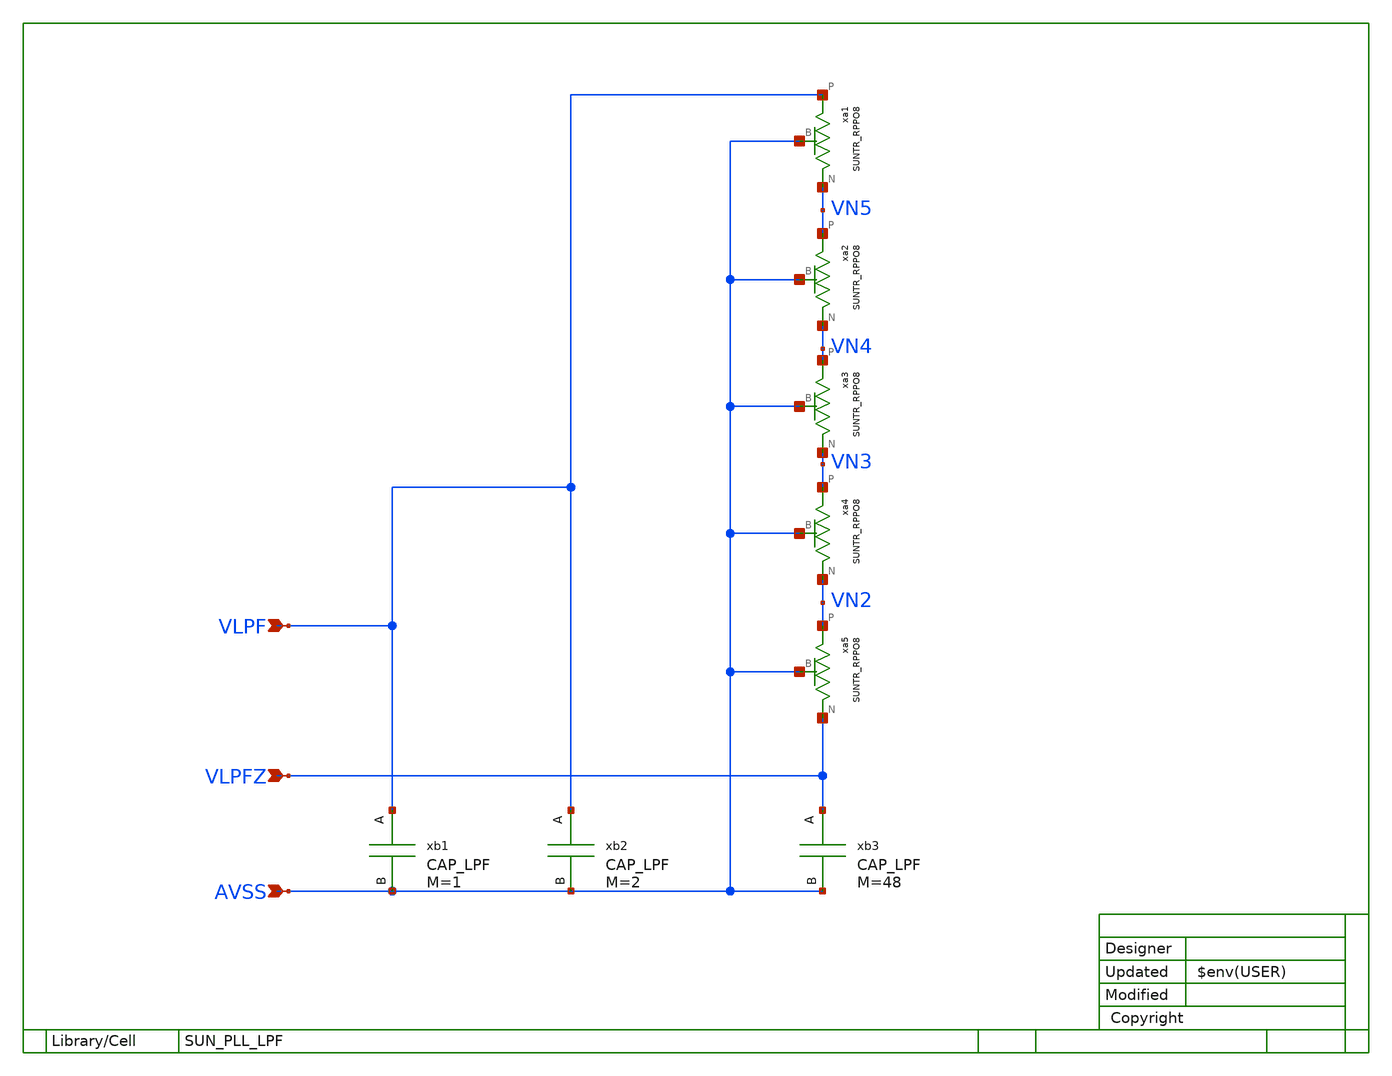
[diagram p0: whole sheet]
** sch_path: ip/sun_pll_sky130nm/design/SUN_PLL_SKY130NM/SUN_PLL_LPF.sch
**.subckt SUN_PLL_LPF VLPF AVSS VLPFZ
*.ipin VLPF
*.ipin AVSS
*.ipin VLPFZ
xa5 VLPFZ VN2 AVSS SUNTR_RPPO8 xoffset=0 yoffset=2 angle=0 M=1
xb3 VLPFZ AVSS CAP_LPF xoffset=0 yoffset=0 angle=0 M=48
xb2 VLPF AVSS CAP_LPF xoffset=0 yoffset=0 angle=0 M=2
xb1 VLPF AVSS CAP_LPF xoffset=0 yoffset=0 angle=0 M=1
xa4 VN2 VN3 AVSS SUNTR_RPPO8 xoffset=0 yoffset=2 angle=0 M=1
xa3 VN3 VN4 AVSS SUNTR_RPPO8 xoffset=0 yoffset=2 angle=0 M=1
xa2 VN4 VN5 AVSS SUNTR_RPPO8 xoffset=0 yoffset=2 angle=0 M=1
xa1 VN5 VLPF AVSS SUNTR_RPPO8 xoffset=0 yoffset=2 angle=0 M=1
**.ends

* expanding   symbol:  SUN_TR_SKY130NM/SUNTR_RPPO8.sym # of pins=3
** sym_path: ip/sun_tr_sky130nm/design/SUN_TR_SKY130NM/SUNTR_RPPO8.sym
** sch_path: ip/sun_tr_sky130nm/design/SUN_TR_SKY130NM/SUNTR_RPPO8.sch
.subckt SUNTR_RPPO8 N P B  xoffset=0 yoffset=0 angle=0 M=1
*.iopin P
*.iopin N
*.iopin B
XXA1 N P B SUNTR_RES8 xoffset=0 yoffset=0 angle=0
.ends


* expanding   symbol:  SUN_PLL_SKY130NM/CAP_LPF.sym # of pins=2
** sym_path: ip/sun_pll_sky130nm/design/SUN_PLL_SKY130NM/CAP_LPF.sym
** sch_path: ip/sun_pll_sky130nm/design/SUN_PLL_SKY130NM/CAP_LPF.sch
.subckt CAP_LPF A B  xoffset=0 yoffset=0 angle=0 M=1
*.iopin A
*.iopin B
R1 A NC0 sky130_fd_pr__res_generic_m1 W=0.4 L=0.4 m=1
R2 B NC1 sky130_fd_pr__res_generic_m1 W=0.4 L=0.4 m=1
.ends


* expanding   symbol:  SUN_TR_SKY130NM/SUNTR_RES8.sym # of pins=3
** sym_path: ip/sun_tr_sky130nm/design/SUN_TR_SKY130NM/SUNTR_RES8.sym
** sch_path: ip/sun_tr_sky130nm/design/SUN_TR_SKY130NM/SUNTR_RES8.sch
.subckt SUNTR_RES8 N P B  xoffset=0 yoffset=0 angle=0
*.iopin N
*.iopin P
*.iopin B
XR1_0 INT_0 N B sky130_fd_pr__res_high_po W=0.72 L=8.8 mult=1 m=1
XR1_1 INT_1 INT_0 B sky130_fd_pr__res_high_po W=0.72 L=8.8 mult=1 m=1
XR1_2 INT_2 INT_1 B sky130_fd_pr__res_high_po W=0.72 L=8.8 mult=1 m=1
XR1_3 INT_3 INT_2 B sky130_fd_pr__res_high_po W=0.72 L=8.8 mult=1 m=1
XR1_4 INT_4 INT_3 B sky130_fd_pr__res_high_po W=0.72 L=8.8 mult=1 m=1
XR1_5 INT_5 INT_4 B sky130_fd_pr__res_high_po W=0.72 L=8.8 mult=1 m=1
XR1_6 INT_6 INT_5 B sky130_fd_pr__res_high_po W=0.72 L=8.8 mult=1 m=1
XR1_7 P INT_6 B sky130_fd_pr__res_high_po W=0.72 L=8.8 mult=1 m=1
.ends

.end
